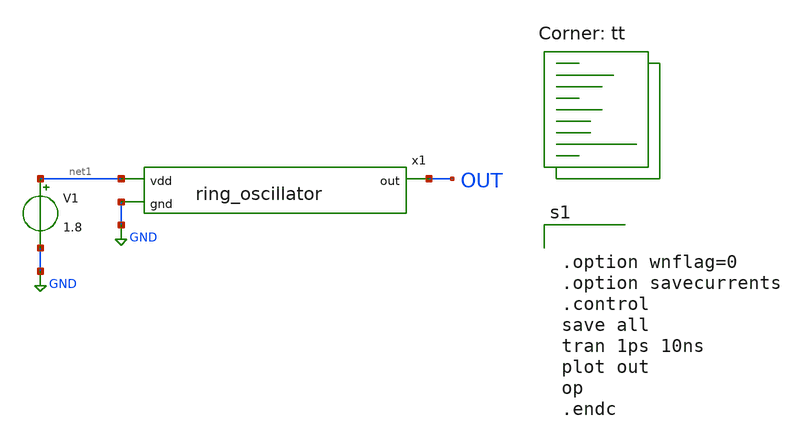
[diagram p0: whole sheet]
** sch_path: xschem/ring_oscillator_tb.sch
**.subckt ring_oscillator_tb
x1 net1 OUT GND ring_oscillator
V1 net1 GND 1.8
**** begin user architecture code
.lib $::SKYWATER_MODELS/sky130.lib.spice tt


.option wnflag=0
.option savecurrents
.control
save all
tran 1ps 10ns
plot out
op
.endc


**** end user architecture code
**.ends
.GLOBAL GND
.end
